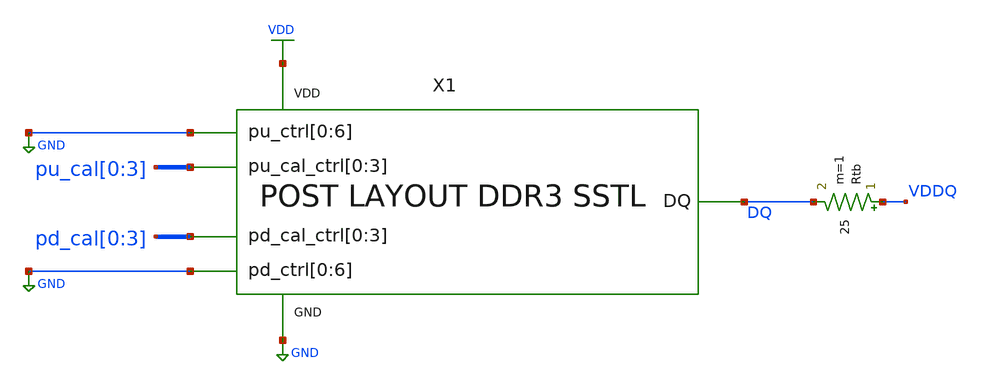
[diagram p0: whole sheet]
** sch_path: schem/post_layout_sstl_cap_tb.sch
* Copyright 2021 Stefan Frederik Schippers
* Licensed under the Apache License, Version 2.0 (the "License");
* you may not use this file except in compliance with the License.
* You may obtain a copy of the License at
* https://www.apache.org/licenses/LICENSE-2.0
* Unless required by applicable law or agreed to in writing, software
* distributed under the License is distributed on an "AS IS" BASIS,
* WITHOUT WARRANTIES OR CONDITIONS OF ANY KIND, either express or implied.
* See the License for the specific language governing permissions and
* limitations under the License.
**.subckt post_layout_sstl_cap_tb
Rtb VDDQ DQ 25 m=1
X1 DQ GND pd_cal[0] pd_cal[1] pd_cal[2] pd_cal[3] GND GND GND GND GND GND GND pu_cal[0] pu_cal[1]
+ pu_cal[2] pu_cal[3] GND GND GND GND GND GND GND VDD SSTL
**** begin user architecture code
 ** Local library links to pdk
.lib ./sky130/libs/SED_process_SED_lib.spice SED_process_SED
.include $::SKYWATER_STDCELLS/sky130_fd_sc_hd.spice
.include ./layout/pex_SSTL.spice

**** end user architecture code
**.ends
.GLOBAL GND
.GLOBAL VDD
**** begin user architecture code


* power voltage
vvdd VDD 0 SED_vdd_SED

** CALIBRATION CONTROL **
* PULLUP
vpu_cal0 pu_cal[0] 0 SED_pucal0_SED
vpu_cal1 pu_cal[1] 0 SED_pucal1_SED
vpu_cal2 pu_cal[2] 0 SED_pucal2_SED
vpu_cal3 pu_cal[3] 0 SED_pucal3_SED
* PULLDOWN
vpd_cal0 pd_cal[0] 0 SED_pdcal0_SED
vpd_cal1 pd_cal[1] 0 SED_pdcal1_SED
vpd_cal2 pd_cal[2] 0 SED_pdcal2_SED
vpd_cal3 pd_cal[3] 0 SED_pdcal3_SED

* INPUT SIGNAL
*                vlow,       vhigh, delay, risetime, falltime, pulsewidth, period, phase
vvddq vddq 0 0 PULSE 0 SED_vdd_SED  0.25n  10p       10p       2n          4n      0

.control
save all
set temp=SED_temp_SED
set num_threads=6

* RUN SIMULATION
tran 1p 4.25n
* Measure rise time
meas tran tdiff_charge    trig at=0.25n targ dq val=SED_vih_SED rise=1
* Measure fall time
meas tran tdiff_discharge trig at=2.25n targ dq val=SED_vil_SED fall=1

* OUTPUT
wrdata ./out/SED_plotName_SED/SED_plotName_SED.txt tdiff_charge tdiff_discharge
set hcopydevtype = svg
hardcopy ./out/SED_plotName_SED/SED_plotName_SED.svg dq vddq title 'DQ vs time'

.endc


**** end user architecture code
.end
